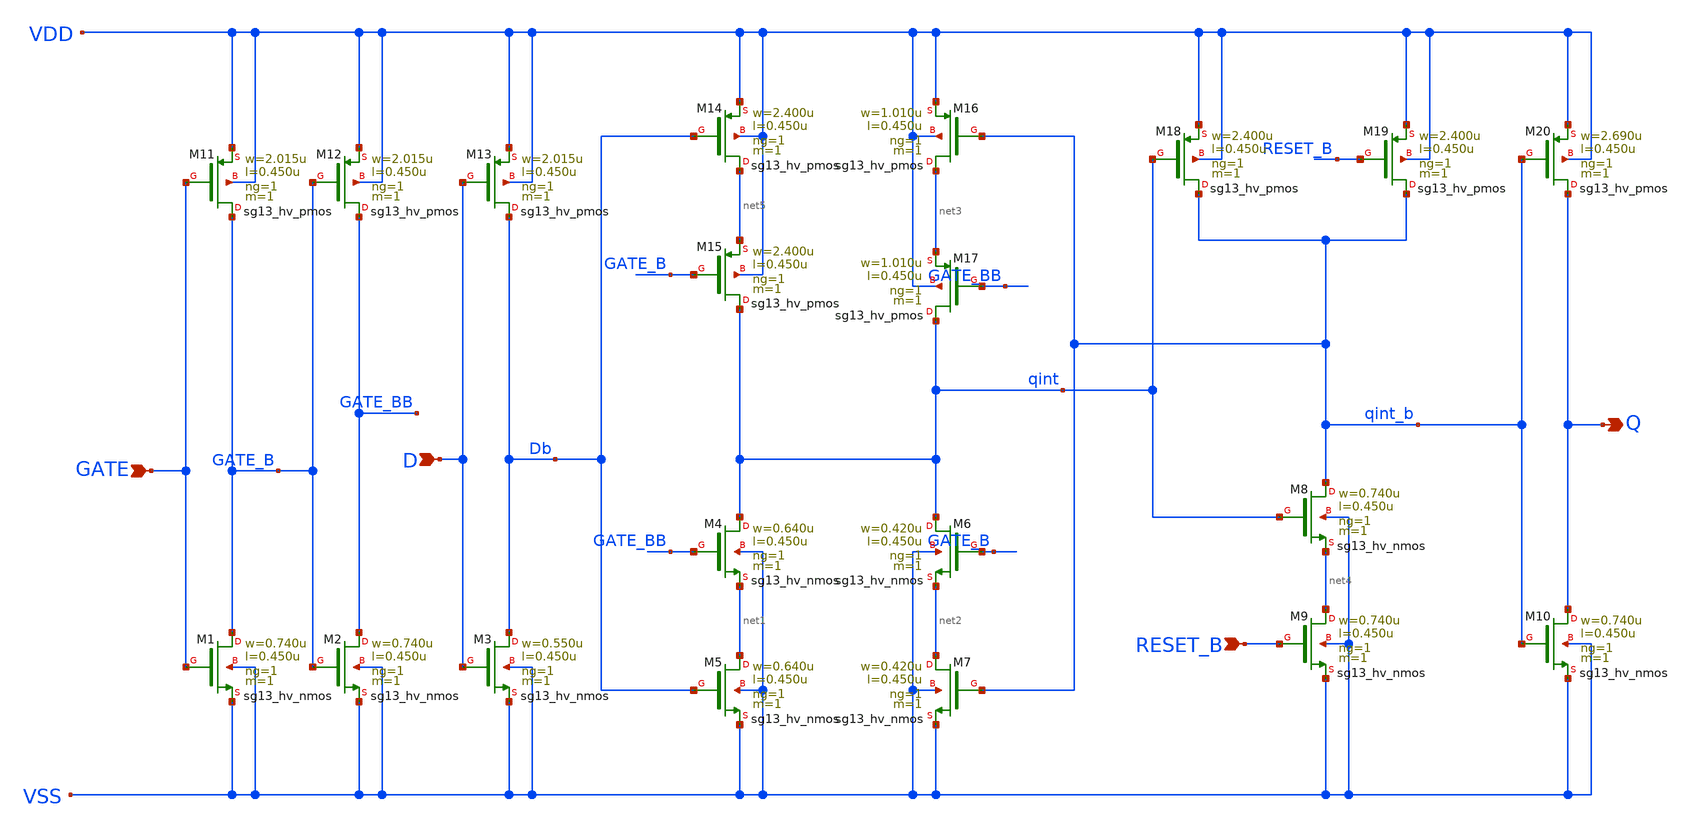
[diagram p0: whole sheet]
** sch_path: ihp-sg13g2/libs.ref/sg13g2_stdcell_hv/sch/xschem/sg13g2_hv_dlhrq_1.sch
* Copyright 2023 IHP PDK Authors
* Licensed under the Apache License, Version 2.0 (the "License");
* you may not use this file except in compliance with the License.
* You may obtain a copy of the License at
* https://www.apache.org/licenses/LICENSE-2.0
* Unless required by applicable law or agreed to in writing, software
* distributed under the License is distributed on an "AS IS" BASIS,
* WITHOUT WARRANTIES OR CONDITIONS OF ANY KIND, either express or implied.
* See the License for the specific language governing permissions and
* limitations under the License.
**.subckt sg13g2_hv_dlhrq_1 D GATE RESET_B Q
*.ipin D
*.ipin GATE
*.ipin RESET_B
*.opin Q
XM1 GATE_B GATE VSS VSS sg13_hv_nmos w=0.740u l=0.450u ng=1 m=1 mm_ok=1
XM2 GATE_BB GATE_B VSS VSS sg13_hv_nmos w=0.740u l=0.450u ng=1 m=1 mm_ok=1
XM3 Db D VSS VSS sg13_hv_nmos w=0.550u l=0.450u ng=1 m=1 mm_ok=1
XM4 qint GATE_BB net1 VSS sg13_hv_nmos w=0.640u l=0.450u ng=1 m=1 mm_ok=1
XM5 net1 Db VSS VSS sg13_hv_nmos w=0.640u l=0.450u ng=1 m=1 mm_ok=1
XM6 qint GATE_B net2 VSS sg13_hv_nmos w=0.420u l=0.450u ng=1 m=1 mm_ok=1
XM7 net2 qint_b VSS VSS sg13_hv_nmos w=0.420u l=0.450u ng=1 m=1 mm_ok=1
XM8 qint_b qint net4 VSS sg13_hv_nmos w=0.740u l=0.450u ng=1 m=1 mm_ok=1
XM9 net4 RESET_B VSS VSS sg13_hv_nmos w=0.740u l=0.450u ng=1 m=1 mm_ok=1
XM10 Q qint_b VSS VSS sg13_hv_nmos w=0.740u l=0.450u ng=1 m=1 mm_ok=1
XM11 GATE_B GATE VDD VDD sg13_hv_pmos w=2.015u l=0.450u ng=1 m=1 mm_ok=1
XM12 GATE_BB GATE_B VDD VDD sg13_hv_pmos w=2.015u l=0.450u ng=1 m=1 mm_ok=1
XM13 Db D VDD VDD sg13_hv_pmos w=2.015u l=0.450u ng=1 m=1 mm_ok=1
XM14 net5 Db VDD VDD sg13_hv_pmos w=2.400u l=0.450u ng=1 m=1 mm_ok=1
XM15 qint GATE_B net5 VDD sg13_hv_pmos w=2.400u l=0.450u ng=1 m=1 mm_ok=1
XM16 net3 qint_b VDD VDD sg13_hv_pmos w=1.010u l=0.450u ng=1 m=1 mm_ok=1
XM17 qint GATE_BB net3 VDD sg13_hv_pmos w=1.010u l=0.450u ng=1 m=1 mm_ok=1
XM18 qint_b qint VDD VDD sg13_hv_pmos w=2.400u l=0.450u ng=1 m=1 mm_ok=1
XM19 qint_b RESET_B VDD VDD sg13_hv_pmos w=2.400u l=0.450u ng=1 m=1 mm_ok=1
XM20 Q qint_b VDD VDD sg13_hv_pmos w=2.690u l=0.450u ng=1 m=1 mm_ok=1
**.ends
.end
